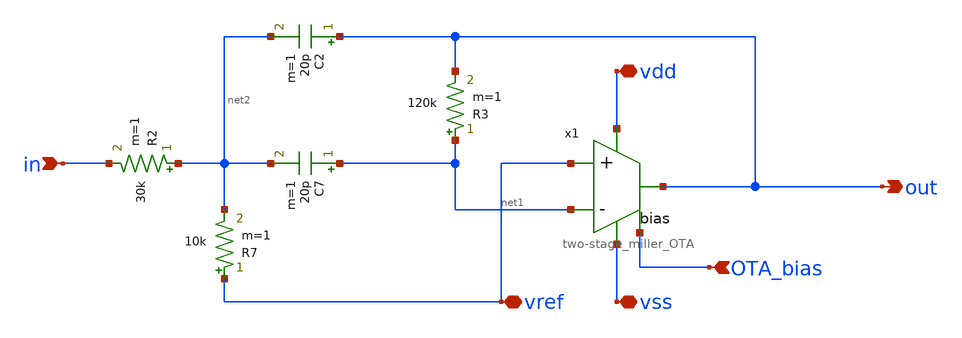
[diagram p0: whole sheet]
** sch_path: design/analog/BPF/BPF.sch
**.subckt BPF out in vdd vss vref OTA_bias
*.opin out
*.ipin in
*.iopin vdd
*.iopin vss
*.iopin vref
*.ipin OTA_bias
R2 net2 in 30k m=1
C2 out net2 20p m=1
R3 net1 out 120k m=1
R7 vref net2 10k m=1
C7 net1 net2 20p m=1
x1 vdd out vref net1 OTA_bias vss two-stage_miller_OTA
**.ends
.end
